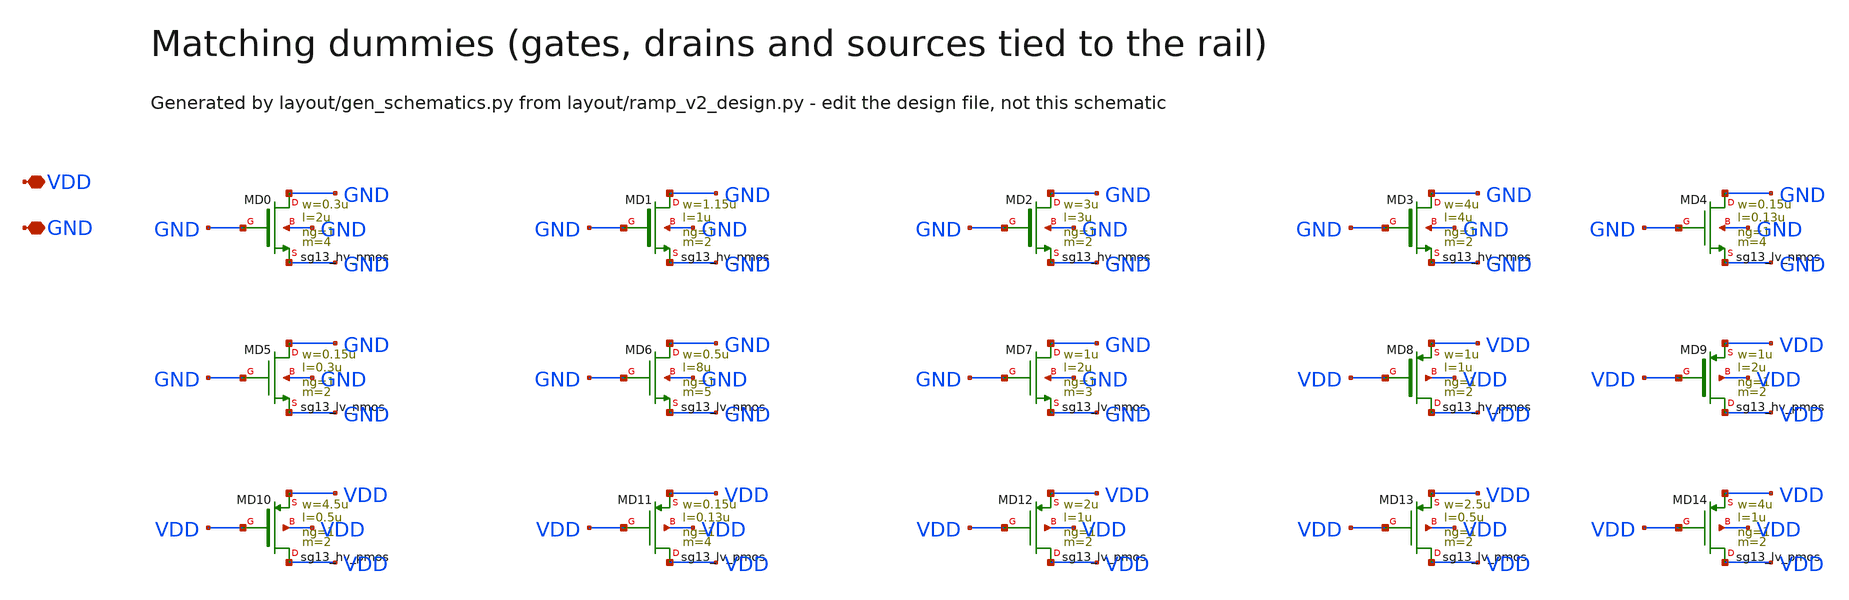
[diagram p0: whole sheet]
** sch_path: Design Files/RAMP/RAMP-V2/DUMMY_V2.sch
**.subckt DUMMY_V2 VDD GND
*.iopin VDD
*.iopin GND
XMD0 GND GND GND GND sg13_hv_nmos w=0.3u l=2u ng=1 m=4 mm_ok=1
XMD1 GND GND GND GND sg13_hv_nmos w=1.15u l=1u ng=1 m=2 mm_ok=1
XMD2 GND GND GND GND sg13_hv_nmos w=3u l=3u ng=1 m=2 mm_ok=1
XMD3 GND GND GND GND sg13_hv_nmos w=4u l=4u ng=1 m=2 mm_ok=1
XMD4 GND GND GND GND sg13_lv_nmos w=0.15u l=0.13u ng=1 m=4 mm_ok=1
XMD5 GND GND GND GND sg13_lv_nmos w=0.15u l=0.3u ng=1 m=2 mm_ok=1
XMD6 GND GND GND GND sg13_lv_nmos w=0.5u l=8u ng=1 m=5 mm_ok=1
XMD7 GND GND GND GND sg13_lv_nmos w=1u l=2u ng=1 m=3 mm_ok=1
XMD8 VDD VDD VDD VDD sg13_hv_pmos w=1u l=1u ng=1 m=2 mm_ok=1
XMD9 VDD VDD VDD VDD sg13_hv_pmos w=1u l=2u ng=1 m=2 mm_ok=1
XMD10 VDD VDD VDD VDD sg13_hv_pmos w=4.5u l=0.5u ng=1 m=2 mm_ok=1
XMD11 VDD VDD VDD VDD sg13_lv_pmos w=0.15u l=0.13u ng=1 m=4 mm_ok=1
XMD12 VDD VDD VDD VDD sg13_lv_pmos w=2u l=1u ng=1 m=2 mm_ok=1
XMD13 VDD VDD VDD VDD sg13_lv_pmos w=2.5u l=0.5u ng=1 m=2 mm_ok=1
XMD14 VDD VDD VDD VDD sg13_lv_pmos w=4u l=1u ng=1 m=2 mm_ok=1
**.ends
.end
